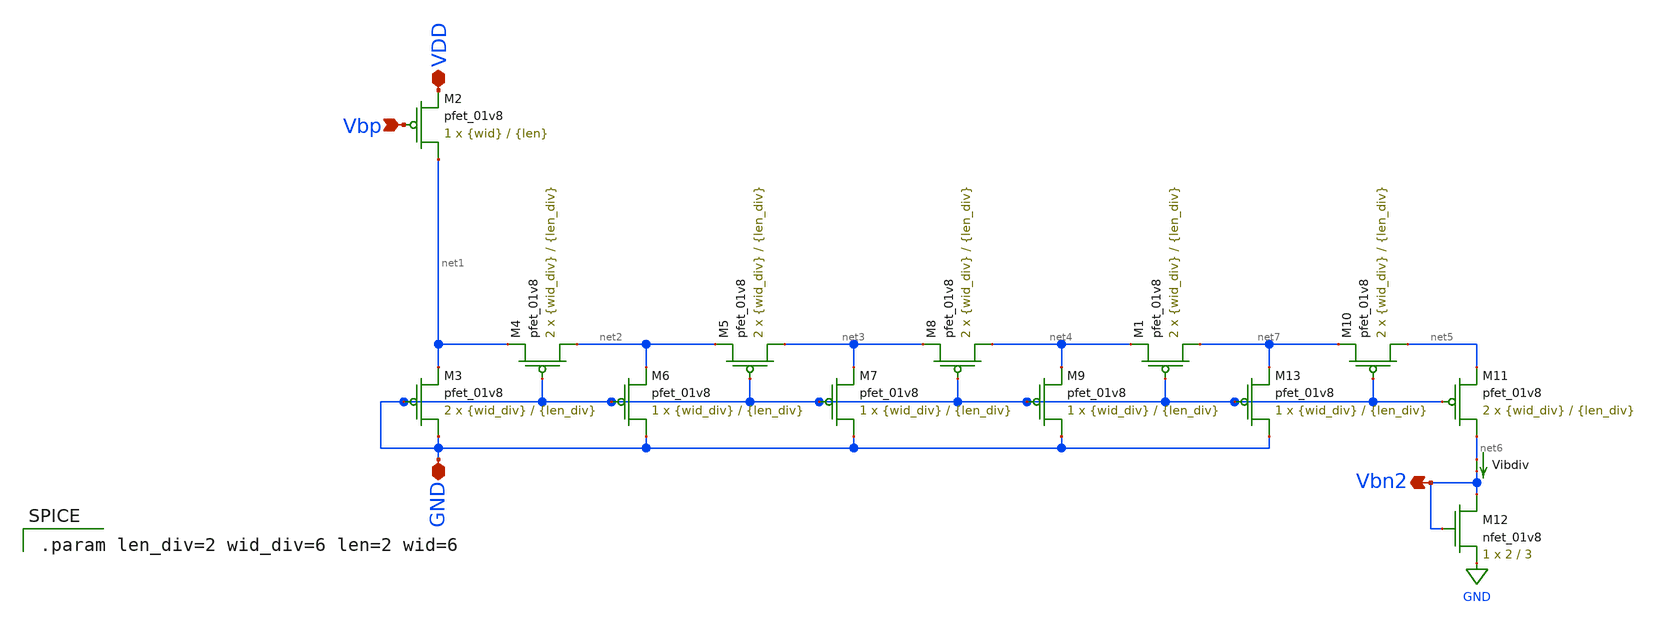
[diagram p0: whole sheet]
** sch_path: mp3/current_divider.sch
**.subckt current_divider GND VDD Vbp Vbn2
*.iopin GND
*.iopin VDD
*.ipin Vbp
*.opin Vbn2
XM2 net1 Vbp VDD VDD sky130_fd_pr__pfet_01v8 L={len} W={wid} nf=1 ad='int((nf+1)/2) * W/nf * 0.29' as='int((nf+2)/2) * W/nf * 0.29'
+ pd='2*int((nf+1)/2) * (W/nf + 0.29)' ps='2*int((nf+2)/2) * (W/nf + 0.29)' nrd='0.29 / W' nrs='0.29 / W'
+ sa=0 sb=0 sd=0 mult=1 m=1
XM3 GND GND net1 VDD sky130_fd_pr__pfet_01v8 L={len_div} W={wid_div} nf=1 ad='int((nf+1)/2) * W/nf * 0.29'
+ as='int((nf+2)/2) * W/nf * 0.29' pd='2*int((nf+1)/2) * (W/nf + 0.29)' ps='2*int((nf+2)/2) * (W/nf + 0.29)'
+ nrd='0.29 / W' nrs='0.29 / W' sa=0 sb=0 sd=0 mult=2 m=2
XM4 net2 GND net1 VDD sky130_fd_pr__pfet_01v8 L={len_div} W={wid_div} nf=1 ad='int((nf+1)/2) * W/nf * 0.29'
+ as='int((nf+2)/2) * W/nf * 0.29' pd='2*int((nf+1)/2) * (W/nf + 0.29)' ps='2*int((nf+2)/2) * (W/nf + 0.29)'
+ nrd='0.29 / W' nrs='0.29 / W' sa=0 sb=0 sd=0 mult=2 m=2
XM6 GND GND net2 VDD sky130_fd_pr__pfet_01v8 L={len_div} W={wid_div} nf=1 ad='int((nf+1)/2) * W/nf * 0.29'
+ as='int((nf+2)/2) * W/nf * 0.29' pd='2*int((nf+1)/2) * (W/nf + 0.29)' ps='2*int((nf+2)/2) * (W/nf + 0.29)'
+ nrd='0.29 / W' nrs='0.29 / W' sa=0 sb=0 sd=0 mult=1 m=1
XM5 net3 GND net2 VDD sky130_fd_pr__pfet_01v8 L={len_div} W={wid_div} nf=1 ad='int((nf+1)/2) * W/nf * 0.29'
+ as='int((nf+2)/2) * W/nf * 0.29' pd='2*int((nf+1)/2) * (W/nf + 0.29)' ps='2*int((nf+2)/2) * (W/nf + 0.29)'
+ nrd='0.29 / W' nrs='0.29 / W' sa=0 sb=0 sd=0 mult=2 m=2
XM7 GND GND net3 VDD sky130_fd_pr__pfet_01v8 L={len_div} W={wid_div} nf=1 ad='int((nf+1)/2) * W/nf * 0.29'
+ as='int((nf+2)/2) * W/nf * 0.29' pd='2*int((nf+1)/2) * (W/nf + 0.29)' ps='2*int((nf+2)/2) * (W/nf + 0.29)'
+ nrd='0.29 / W' nrs='0.29 / W' sa=0 sb=0 sd=0 mult=1 m=1
XM8 net4 GND net3 VDD sky130_fd_pr__pfet_01v8 L={len_div} W={wid_div} nf=1 ad='int((nf+1)/2) * W/nf * 0.29'
+ as='int((nf+2)/2) * W/nf * 0.29' pd='2*int((nf+1)/2) * (W/nf + 0.29)' ps='2*int((nf+2)/2) * (W/nf + 0.29)'
+ nrd='0.29 / W' nrs='0.29 / W' sa=0 sb=0 sd=0 mult=2 m=2
XM9 GND GND net4 VDD sky130_fd_pr__pfet_01v8 L={len_div} W={wid_div} nf=1 ad='int((nf+1)/2) * W/nf * 0.29'
+ as='int((nf+2)/2) * W/nf * 0.29' pd='2*int((nf+1)/2) * (W/nf + 0.29)' ps='2*int((nf+2)/2) * (W/nf + 0.29)'
+ nrd='0.29 / W' nrs='0.29 / W' sa=0 sb=0 sd=0 mult=1 m=1
XM10 net5 GND net7 VDD sky130_fd_pr__pfet_01v8 L={len_div} W={wid_div} nf=1 ad='int((nf+1)/2) * W/nf * 0.29'
+ as='int((nf+2)/2) * W/nf * 0.29' pd='2*int((nf+1)/2) * (W/nf + 0.29)' ps='2*int((nf+2)/2) * (W/nf + 0.29)'
+ nrd='0.29 / W' nrs='0.29 / W' sa=0 sb=0 sd=0 mult=2 m=2
XM11 net6 GND net5 VDD sky130_fd_pr__pfet_01v8 L={len_div} W={wid_div} nf=1 ad='int((nf+1)/2) * W/nf * 0.29'
+ as='int((nf+2)/2) * W/nf * 0.29' pd='2*int((nf+1)/2) * (W/nf + 0.29)' ps='2*int((nf+2)/2) * (W/nf + 0.29)'
+ nrd='0.29 / W' nrs='0.29 / W' sa=0 sb=0 sd=0 mult=2 m=2
XM12 Vbn2 Vbn2 GND GND sky130_fd_pr__nfet_01v8 L=3 W=2 nf=1 ad='int((nf+1)/2) * W/nf * 0.29' as='int((nf+2)/2) * W/nf * 0.29'
+ pd='2*int((nf+1)/2) * (W/nf + 0.29)' ps='2*int((nf+2)/2) * (W/nf + 0.29)' nrd='0.29 / W' nrs='0.29 / W'
+ sa=0 sb=0 sd=0 mult=1 m=1
Vibdiv net6 Vbn2 0
.save i(vibdiv)
XM1 net7 GND net4 VDD sky130_fd_pr__pfet_01v8 L={len_div} W={wid_div} nf=1 ad='int((nf+1)/2) * W/nf * 0.29'
+ as='int((nf+2)/2) * W/nf * 0.29' pd='2*int((nf+1)/2) * (W/nf + 0.29)' ps='2*int((nf+2)/2) * (W/nf + 0.29)'
+ nrd='0.29 / W' nrs='0.29 / W' sa=0 sb=0 sd=0 mult=2 m=2
XM13 GND GND net7 VDD sky130_fd_pr__pfet_01v8 L={len_div} W={wid_div} nf=1 ad='int((nf+1)/2) * W/nf * 0.29'
+ as='int((nf+2)/2) * W/nf * 0.29' pd='2*int((nf+1)/2) * (W/nf + 0.29)' ps='2*int((nf+2)/2) * (W/nf + 0.29)'
+ nrd='0.29 / W' nrs='0.29 / W' sa=0 sb=0 sd=0 mult=1 m=1
**** begin user architecture code

.param len_div=2 wid_div=6 len=2 wid=6

**** end user architecture code
**.ends
.GLOBAL GND
.end
